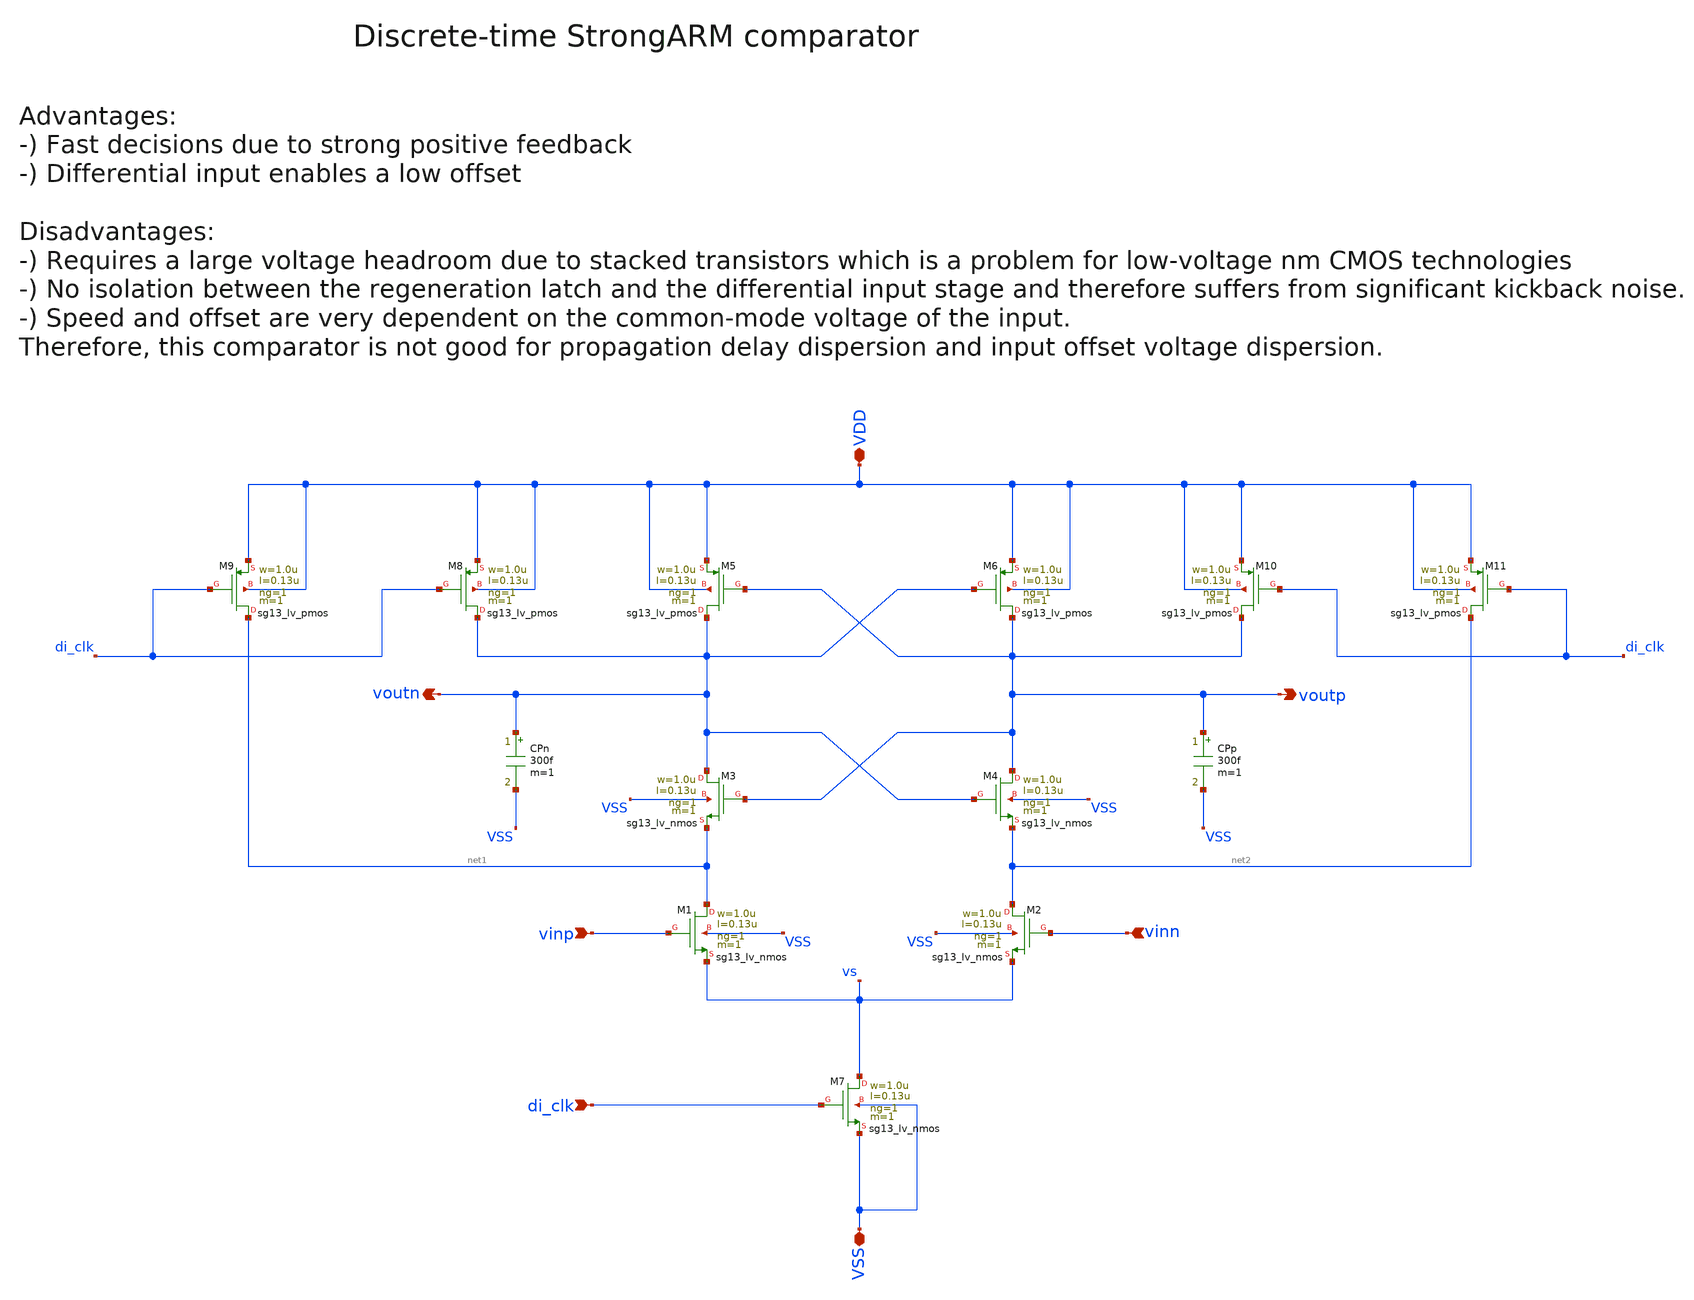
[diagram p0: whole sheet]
** sch_path: SG13G2_ATBS-ADC-main/xschem/comparator/discrete_time/StrongARM/StrongARM_comparator.sch
**.subckt StrongARM_comparator VDD voutp VSS voutn vinp vinn di_clk
*.iopin VDD
*.opin voutp
*.iopin VSS
*.opin voutn
*.ipin vinp
*.ipin vinn
*.ipin di_clk
XM1 net1 vinp vs VSS sg13_lv_nmos w=1.0u l=0.13u ng=1 m=1 mm_ok=1
XM2 net2 vinn vs VSS sg13_lv_nmos w=1.0u l=0.13u ng=1 m=1 mm_ok=1
XM3 voutn voutp net1 VSS sg13_lv_nmos w=1.0u l=0.13u ng=1 m=1 mm_ok=1
XM4 voutp voutn net2 VSS sg13_lv_nmos w=1.0u l=0.13u ng=1 m=1 mm_ok=1
XM5 voutn voutp VDD VDD sg13_lv_pmos w=1.0u l=0.13u ng=1 m=1 mm_ok=1
XM6 voutp voutn VDD VDD sg13_lv_pmos w=1.0u l=0.13u ng=1 m=1 mm_ok=1
XM7 vs di_clk VSS VSS sg13_lv_nmos w=1.0u l=0.13u ng=1 m=1 mm_ok=1
XM8 voutn di_clk VDD VDD sg13_lv_pmos w=1.0u l=0.13u ng=1 m=1 mm_ok=1
XM9 net1 di_clk VDD VDD sg13_lv_pmos w=1.0u l=0.13u ng=1 m=1 mm_ok=1
XM10 voutp di_clk VDD VDD sg13_lv_pmos w=1.0u l=0.13u ng=1 m=1 mm_ok=1
XM11 net2 di_clk VDD VDD sg13_lv_pmos w=1.0u l=0.13u ng=1 m=1 mm_ok=1
CPn voutn VSS 300f m=1
CPp voutp VSS 300f m=1
**.ends
.end
